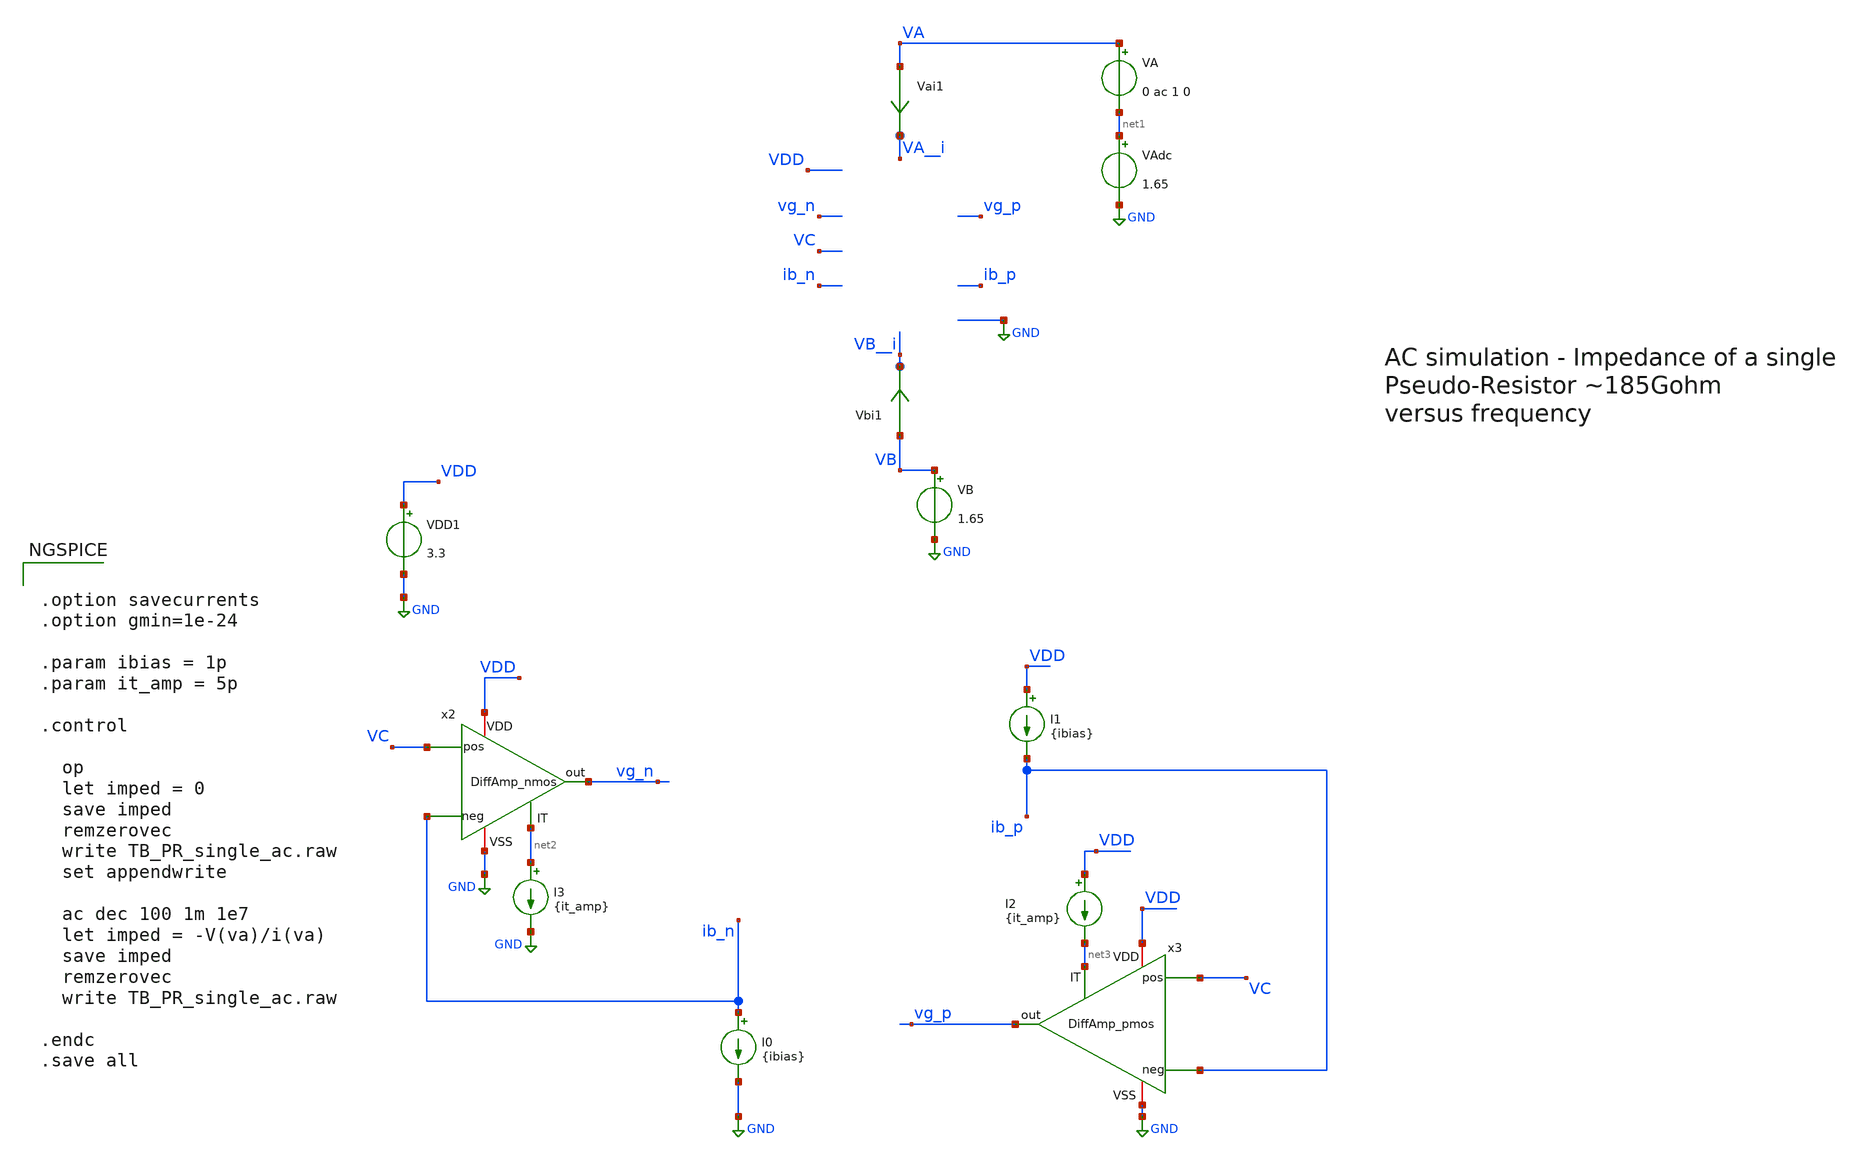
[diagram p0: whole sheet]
** sch_path: TIA/xschem/PseudoResistor/TB_PR_single_ac.sch
**.subckt TB_PR_single_ac
VDD1 VDD GND 3.3
VA VA net1 0 ac 1 0
VB VB GND 1.65
VAdc net1 GND 1.65
Vai1 VA VA__i 0
.save i(vai1)
Vbi1 VB VB__i 0
.save i(vbi1)
I0 ib_n GND {ibias}
I1 VDD ib_p {ibias}
x2 VDD GND VC ib_n net2 vg_n DiffAmp_nmos
I2 VDD net3 {it_amp}
x3 VDD GND net3 ib_p VC vg_p DiffAmp_pmos
I3 net2 GND {it_amp}
**** begin user architecture code


.option savecurrents
.option gmin=1e-24

.param ibias = 1p
.param it_amp = 5p

.control

  op
  let imped = 0
  save imped
  remzerovec
  write TB_PR_single_ac.raw
  set appendwrite

  ac dec 100 1m 1e7
  let imped = -V(va)/i(va)
  save imped
  remzerovec
  write TB_PR_single_ac.raw

.endc
.save all



.include $::180MCU_MODELS/design.ngspice
.lib $::180MCU_MODELS/sm141064.ngspice typical

.include /home/gmaranhao/Desktop/gf180_work/TIA/PseudoResistor/layout/spice/PR_net_pex.spice

*.subckt PR_net VDD VSS VB VC VA VG_N IB_N IB_P VG_P
X1 VDD 0 VB__i VC VA__i vg_n ib_n ib_p vg_p PR_net


**** end user architecture code
**.ends
.GLOBAL GND
.end
